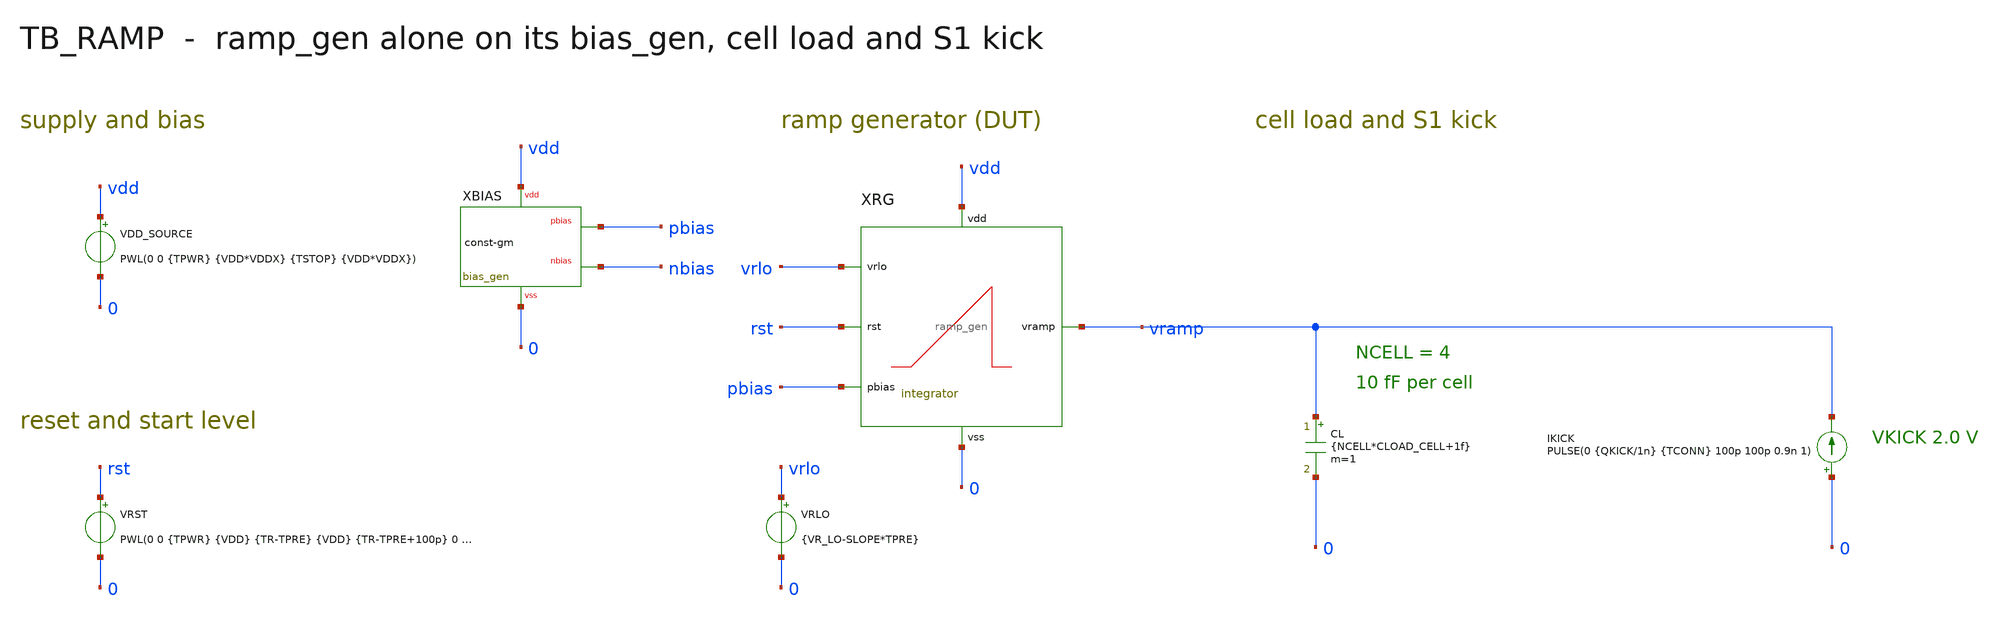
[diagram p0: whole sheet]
** sch_path: mixed_signal/ramp_gen/tb_ramp.sch
**.subckt tb_ramp
VDD_SOURCE vdd 0 PWL(0 0 {TPWR} {VDD*VDDX} {TSTOP} {VDD*VDDX})
XBIAS vdd 0 pbias nbias bias_gen
VRST rst 0 PWL(0 0 {TPWR} {VDD} {TR-TPRE} {VDD} {TR-TPRE+100p} 0 {TRST2} 0 {TRST2+100p} {VDD})
VRLO vrlo 0 {VR_LO-SLOPE*TPRE}
XRG vramp rst vrlo pbias vdd 0 ramp_gen
CL vramp 0 {NCELL*CLOAD_CELL+1f} m=1
IKICK 0 vramp PULSE(0 {QKICK/1n} {TCONN} 100p 100p 0.9n 1)
**** begin user architecture code

.include /foss/pdks/gf180mcuD/libs.tech/ngspice/design.ngspice
.lib /foss/pdks/gf180mcuD/libs.tech/ngspice/sm141064.ngspice typical
.lib /foss/pdks/gf180mcuD/libs.tech/ngspice/sm141064.ngspice res_typical
.lib /foss/pdks/gf180mcuD/libs.tech/ngspice/sm141064.ngspice mimcap_typical
.lib /foss/pdks/gf180mcuD/libs.tech/ngspice/sm141064.ngspice moscap_typical
.include /foss/designs/mixed_signal/ramp_gen/ref/bias_gen/data/bias_gen_params.spice
.include /foss/designs/mixed_signal/ramp_gen/ref/bias_gen/bias_gen.spice
.include /foss/designs/mixed_signal/ramp_gen/data/ramp_gen_params.spice


.param VDD=3.3
.param TCOUNT=50n
.param VR_LO=0.5
.param VR_HI=2.0
.param LSB='(VR_HI-VR_LO)/256'
.param TRAMP='256*TCOUNT'
.param SLOPE='(VR_HI-VR_LO)/TRAMP'
.param CLOAD_CELL=10f
.param NCELL=4
.param VKICK=2.0
.param VDDX=1
.param TPRE=0
.param TPWR=100n
.param T0=1u
.param TS='T0+300n'
.param TCONN='TS+10n'
.param TR='T0+400n'
.param TE='TR+TRAMP'
.param TOVR='20*TCOUNT'
.param TRST2='TE+TOVR+50n'
.param TSTOP='TRST2+600n'
.param QKICK='NCELL*CLOAD_CELL*(VKICK-VR_LO)'


.options reltol=1e-5 abstol=1e-13 vntol=1e-7 gmin=1e-15 savecurrents
.tran 0.2n {TSTOP} 0 2n
.save v(vramp) v(xrg.vx) v(rst) v(pbias) v(xrg.d2) v(xrg.nd) i(vdd_source)
.save @m.xrg.xns.m0[vds] @m.xrg.xns.m0[vdsat] @m.xrg.xps.m0[vds] @m.xrg.xps.m0[vdsat]
.save @m.xrg.xm5.m0[vds] @m.xrg.xm5.m0[vdsat] @m.xrg.xm6.m0[vds] @m.xrg.xm6.m0[vdsat]
.save @m.xrg.xm7.m0[vds] @m.xrg.xm7.m0[vdsat] @m.xrg.xm1.m0[vds] @m.xrg.xm1.m0[vdsat]
.save @m.xrg.xns.m0[id] @m.xrg.xps.m0[id] @m.xrg.xm5.m0[id] @m.xrg.xm6.m0[id] @m.xrg.xm7.m0[id]
.measure tran vr_tconn FIND v(vramp) AT={TCONN}
.measure tran vr_kick_max MAX v(vramp) FROM={TCONN} TO={TR}
.measure tran vr_tr FIND v(vramp) AT={TR}
.measure tran vx_tr FIND v(xrg.vx) AT={TR}
.measure tran vx_mid FIND v(xrg.vx) AT={TR+TRAMP/2}
.measure tran vx_te FIND v(xrg.vx) AT={TE}
.measure tran vr_te FIND v(vramp) AT={TE}
.measure tran vr_ovr FIND v(vramp) AT={TE+TOVR}
.measure tran i_ns AVG @m.xrg.xns.m0[id] FROM={TR} TO={TE}
.measure tran i_ps AVG @m.xrg.xps.m0[id] FROM={TR} TO={TE}
.measure tran i_m5 AVG @m.xrg.xm5.m0[id] FROM={TR} TO={TE}
.measure tran i_m7 AVG @m.xrg.xm7.m0[id] FROM={TR} TO={TE}
.measure tran i_total AVG i(vdd_source) FROM={TR} TO={TE}
.measure tran ns_vds_min MIN @m.xrg.xns.m0[vds] FROM={TR} TO={TE+TOVR}
.measure tran ns_vdsat FIND @m.xrg.xns.m0[vdsat] AT={TR}
.measure tran ns_margin PARAM='ns_vds_min-ns_vdsat'
.measure tran m5_vds_min MIN @m.xrg.xm5.m0[vds] FROM={TR} TO={TE+TOVR}
.measure tran m5_vdsat FIND @m.xrg.xm5.m0[vdsat] AT={TR}
.measure tran m5_margin PARAM='m5_vds_min-m5_vdsat'
.measure tran m6_vds_maxabs MIN @m.xrg.xm6.m0[vds] FROM={TR} TO={TE+TOVR}
.measure tran m6_vdsat FIND @m.xrg.xm6.m0[vdsat] AT={TE+TOVR}
.measure tran m7_vds FIND @m.xrg.xm7.m0[vds] AT={TR}
.measure tran m7_vdsat FIND @m.xrg.xm7.m0[vdsat] AT={TR}
.measure tran m1_vds FIND @m.xrg.xm1.m0[vds] AT={TR}
.measure tran m1_vdsat FIND @m.xrg.xm1.m0[vdsat] AT={TR}
.measure tran ps_vds FIND @m.xrg.xps.m0[vds] AT={TR}
.measure tran ps_vdsat FIND @m.xrg.xps.m0[vdsat] AT={TR}
.measure tran pbias_tr FIND v(pbias) AT={TR}
.measure tran pbias_min MIN v(pbias) FROM={TR} TO={TSTOP}
.measure tran pbias_max MAX v(pbias) FROM={TR} TO={TSTOP}
.control
set num_threads=1
set wr_singlescale
set wr_vecnames
run
wrdata ramp.csv v(vramp) v(xrg.vx) v(rst) v(pbias)
quit
.endc

**** end user architecture code
**.ends
.end
